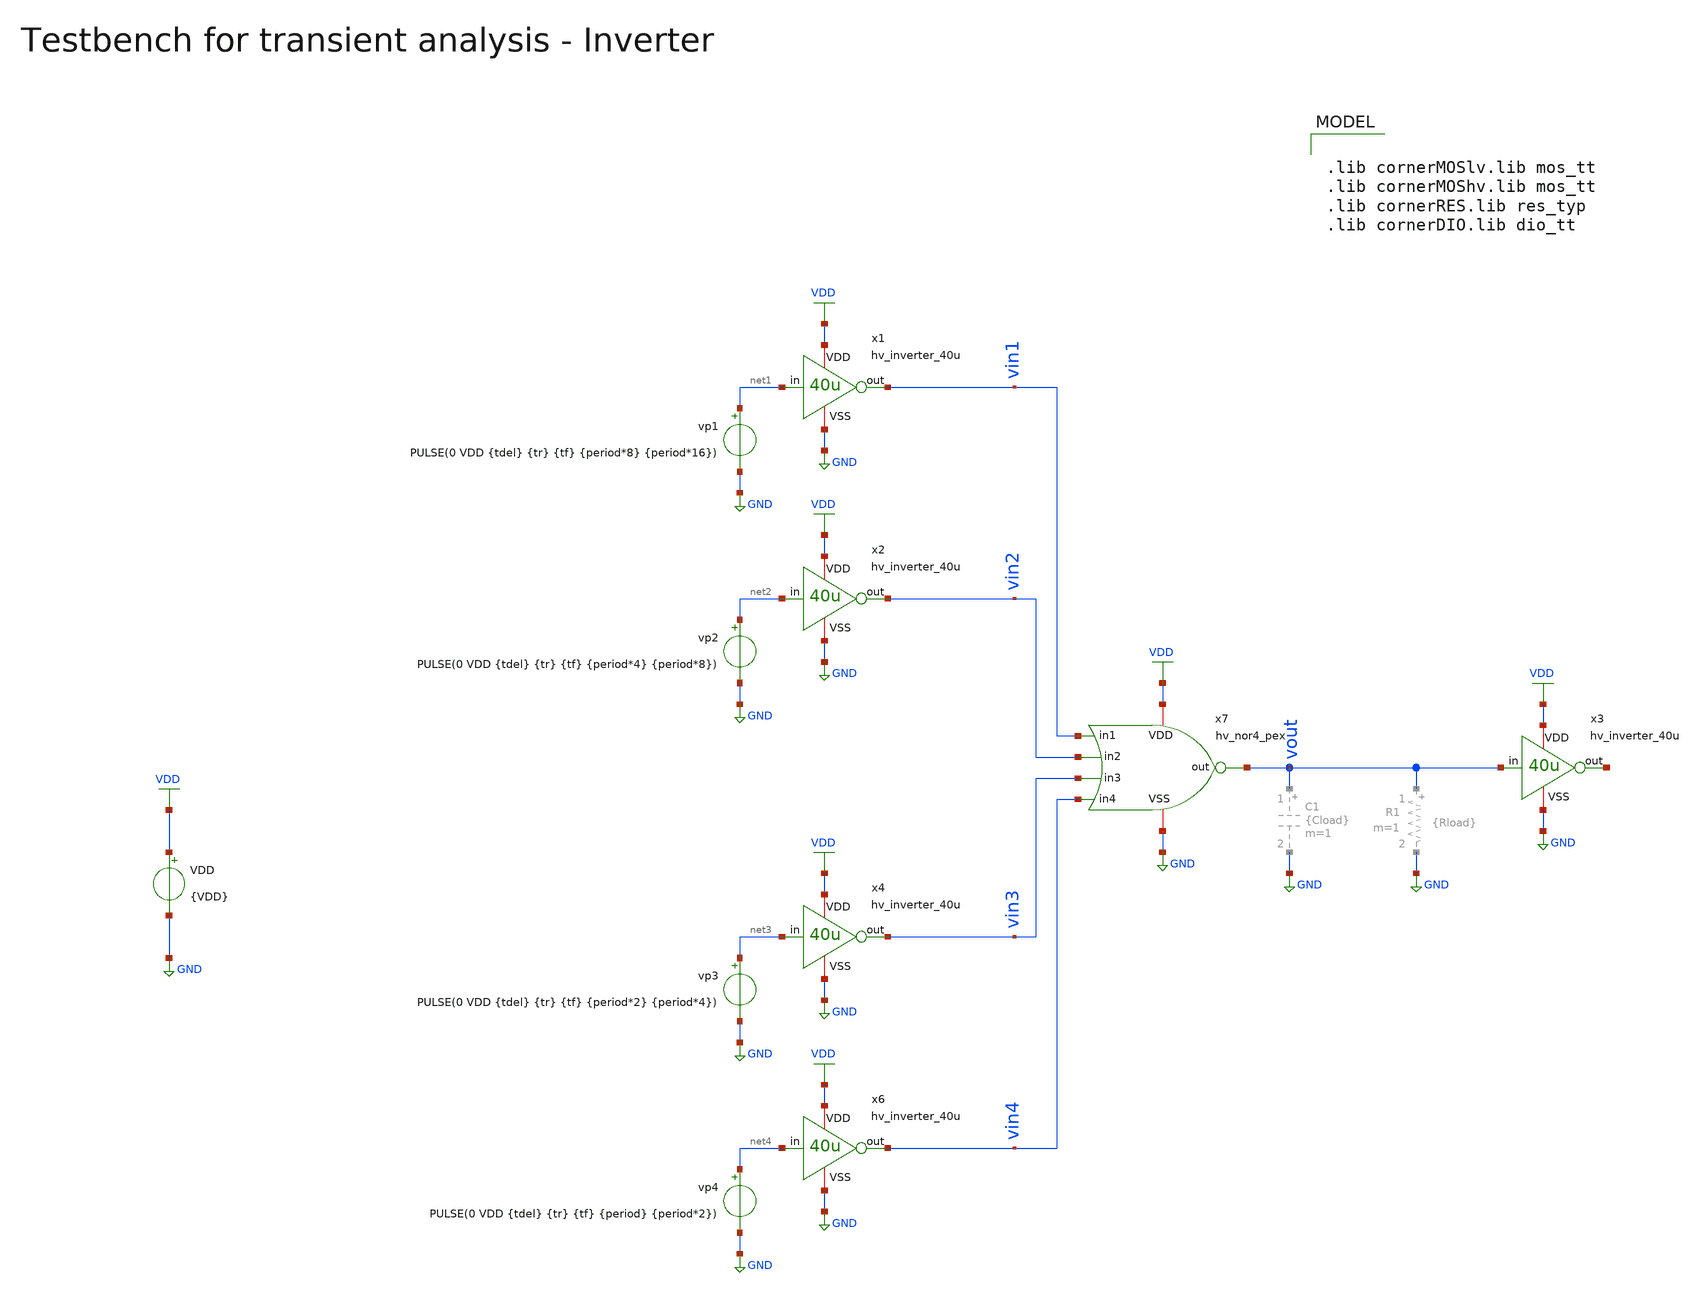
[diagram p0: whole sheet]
** sch_path: macros/heichips26_vcr/macros/switched_capacitor/testbenches/xschem/tb_hv_nor4_pex_tran.sch
**.subckt tb_hv_nor4_pex_tran
VDD VDD GND {VDD}
vp2 net2 GND PULSE(0 VDD {tdel} {tr} {tf} {period*4} {period*8})
vp1 net1 GND PULSE(0 VDD {tdel} {tr} {tf} {period*8} {period*16})
x1 VDD net1 vin1 GND hv_inverter_40u
x2 VDD net2 vin2 GND hv_inverter_40u
x3 VDD vout net5 GND hv_inverter_40u
vp3 net3 GND PULSE(0 VDD {tdel} {tr} {tf} {period*2} {period*4})
x4 VDD net3 vin3 GND hv_inverter_40u
vp4 net4 GND PULSE(0 VDD {tdel} {tr} {tf} {period} {period*2})
x6 VDD net4 vin4 GND hv_inverter_40u
x7 VDD vin1 vout vin2 GND vin3 vin4 hv_nor4_pex
**** begin user architecture code


.include ../../../netlist/pex/hv_nor4_magic_pex_3.spice
.param VDD=3.3
.csparam VDD=VDD
.param Vcm=VDD/2
.param temp=27
.param Cload=10p
.param Rload=1k

.param period = 1n
.param tdel   = {period/2}
.param ton    = {period*2}
.csparam tstop  = {17*period}
.csparam tstep  = {period/100}
.param tr     = {period/100}
.param tf     = {period/100}

.options savecurrents klu method=gear reltol=1e-4 abstol=1e-15 gmin=1e-15
.control

save all

* Operating Point Analysis
op
remzerovec
write @schname\.raw
set appendwrite

* Transient Analysis
tran {$&tstep} {$&tstop}
write @schname\.raw

* Plotting
plot vin1+16 vin2+12 vin3+8 vin4+4 vout

* Write Data
unset appendwrite
set wr_vecnames
set wr_singlescale
wrdata ../plot_simulations/data/@schname\.txt v(vin1) v(vin2) v(vout)

*quit
.endc



.lib cornerMOSlv.lib mos_tt
.lib cornerMOShv.lib mos_tt
.lib cornerRES.lib res_typ
.lib cornerDIO.lib dio_tt

**** end user architecture code
**.ends

* expanding   symbol:  hv_inverter_40u.sym # of pins=4
** sym_path: macros/heichips26_vcr/macros/switched_capacitor/schematic/xschem/hv_inverter_40u.sym
** sch_path: macros/heichips26_vcr/macros/switched_capacitor/schematic/xschem/hv_inverter_40u.sch
.subckt hv_inverter_40u VDD in out VSS
*.ipin in
*.iopin VDD
*.iopin VSS
*.opin out
XM2 out in VSS VSS sg13_hv_nmos w={n_w} l={n_l} ng={ng} m=1 mm_ok=1
XM3 out in VDD VDD sg13_hv_pmos w={p_w} l={p_l} ng={ng} m=1 mm_ok=1
**** begin user architecture code


.param w   = 10u
.param ng  = 4
.param n_ng = ng
.param n_w = {3u*n_ng}
.param n_l = 0.45u
.param p_ng = ng
.param p_w = {10u*p_ng}
.param p_l = 0.4u


**** end user architecture code
.ends

.GLOBAL GND
.GLOBAL VDD
.end
